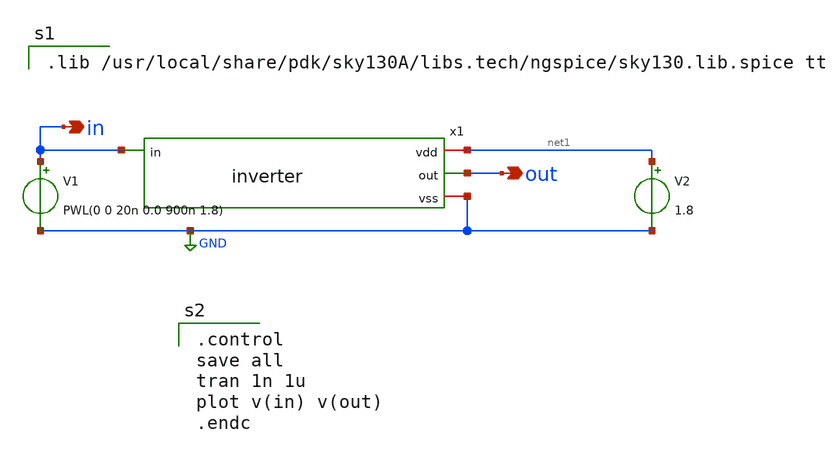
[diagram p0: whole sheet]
** sch_path: xschem/inverter_tb.sch
**.subckt inverter_tb out in
*.opin out
*.opin in
x1 net1 out in GND inverter
V1 in GND PWL(0 0 20n 0.0 900n 1.8)
V2 net1 GND 1.8
**** begin user architecture code

.lib /usr/local/share/pdk/sky130A/libs.tech/ngspice/sky130.lib.spice tt


.control
save all
tran 1n 1u
plot v(in) v(out)
.endc

**** end user architecture code
**.ends

* expanding   symbol:  inverter.sym # of pins=4
** sym_path: xschem/inverter.sym
** sch_path: xschem/inverter.sch
.subckt inverter vdd out in vss
*.iopin vdd
*.iopin vss
*.opin out
*.ipin in
XM1 out in vss vss sky130_fd_pr__nfet_01v8 L=0.18 W=4.5 nf=3 ad='int((nf+1)/2) * W/nf * 0.29' as='int((nf+2)/2) * W/nf * 0.29'
+ pd='2*int((nf+1)/2) * (W/nf + 0.29)' ps='2*int((nf+2)/2) * (W/nf + 0.29)' nrd='0.29 / W' nrs='0.29 / W'
+ sa=0 sb=0 sd=0 mult=1 m=1
XM2 out in vdd vdd sky130_fd_pr__pfet_01v8 L=0.18 W=3 nf=3 ad='int((nf+1)/2) * W/nf * 0.29' as='int((nf+2)/2) * W/nf * 0.29'
+ pd='2*int((nf+1)/2) * (W/nf + 0.29)' ps='2*int((nf+2)/2) * (W/nf + 0.29)' nrd='0.29 / W' nrs='0.29 / W'
+ sa=0 sb=0 sd=0 mult=1 m=1
.ends

.GLOBAL GND
.end
